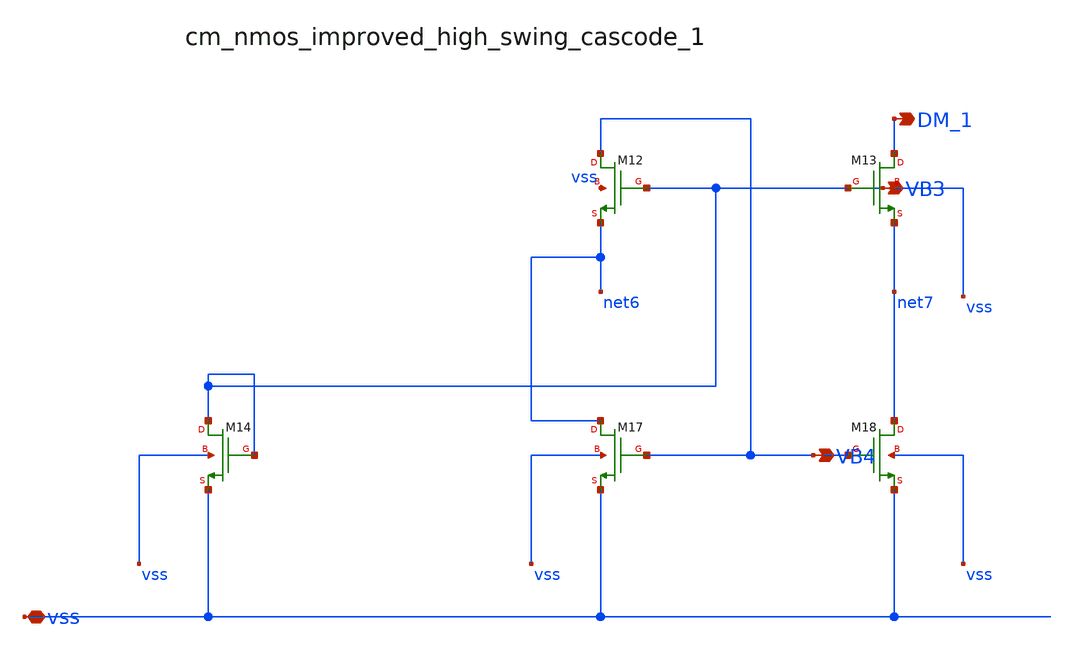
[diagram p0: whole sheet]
** sch_path: analog-db/raw/amp_017_tan_clia/hier/blocks/cm_nmos_improved_high_swing_cascode_1.sch
**.subckt cm_nmos_improved_high_swing_cascode_1 vss VB4 DM_1 VB3
*.iopin vss
*.opin VB4
*.opin DM_1
*.opin VB3
XM12 VB4 VB3 net6 vss sg13_lv_nmos w=x_dut_xm12_w l=x_dut_xm12_l ng=1 m=x_dut_xm12_m
XM13 DM_1 VB3 net7 vss sg13_lv_nmos w=x_dut_xm13_w l=x_dut_xm13_l ng=1 m=x_dut_xm13_m
XM14 VB3 VB3 vss vss sg13_lv_nmos w=x_dut_xm14_w l=x_dut_xm14_l ng=1 m=x_dut_xm14_m
XM17 net6 VB4 vss vss sg13_lv_nmos w=x_dut_xm17_w l=x_dut_xm17_l ng=1 m=x_dut_xm17_m
XM18 net7 VB4 vss vss sg13_lv_nmos w=x_dut_xm18_w l=x_dut_xm18_l ng=1 m=x_dut_xm18_m
**.ends
.end
